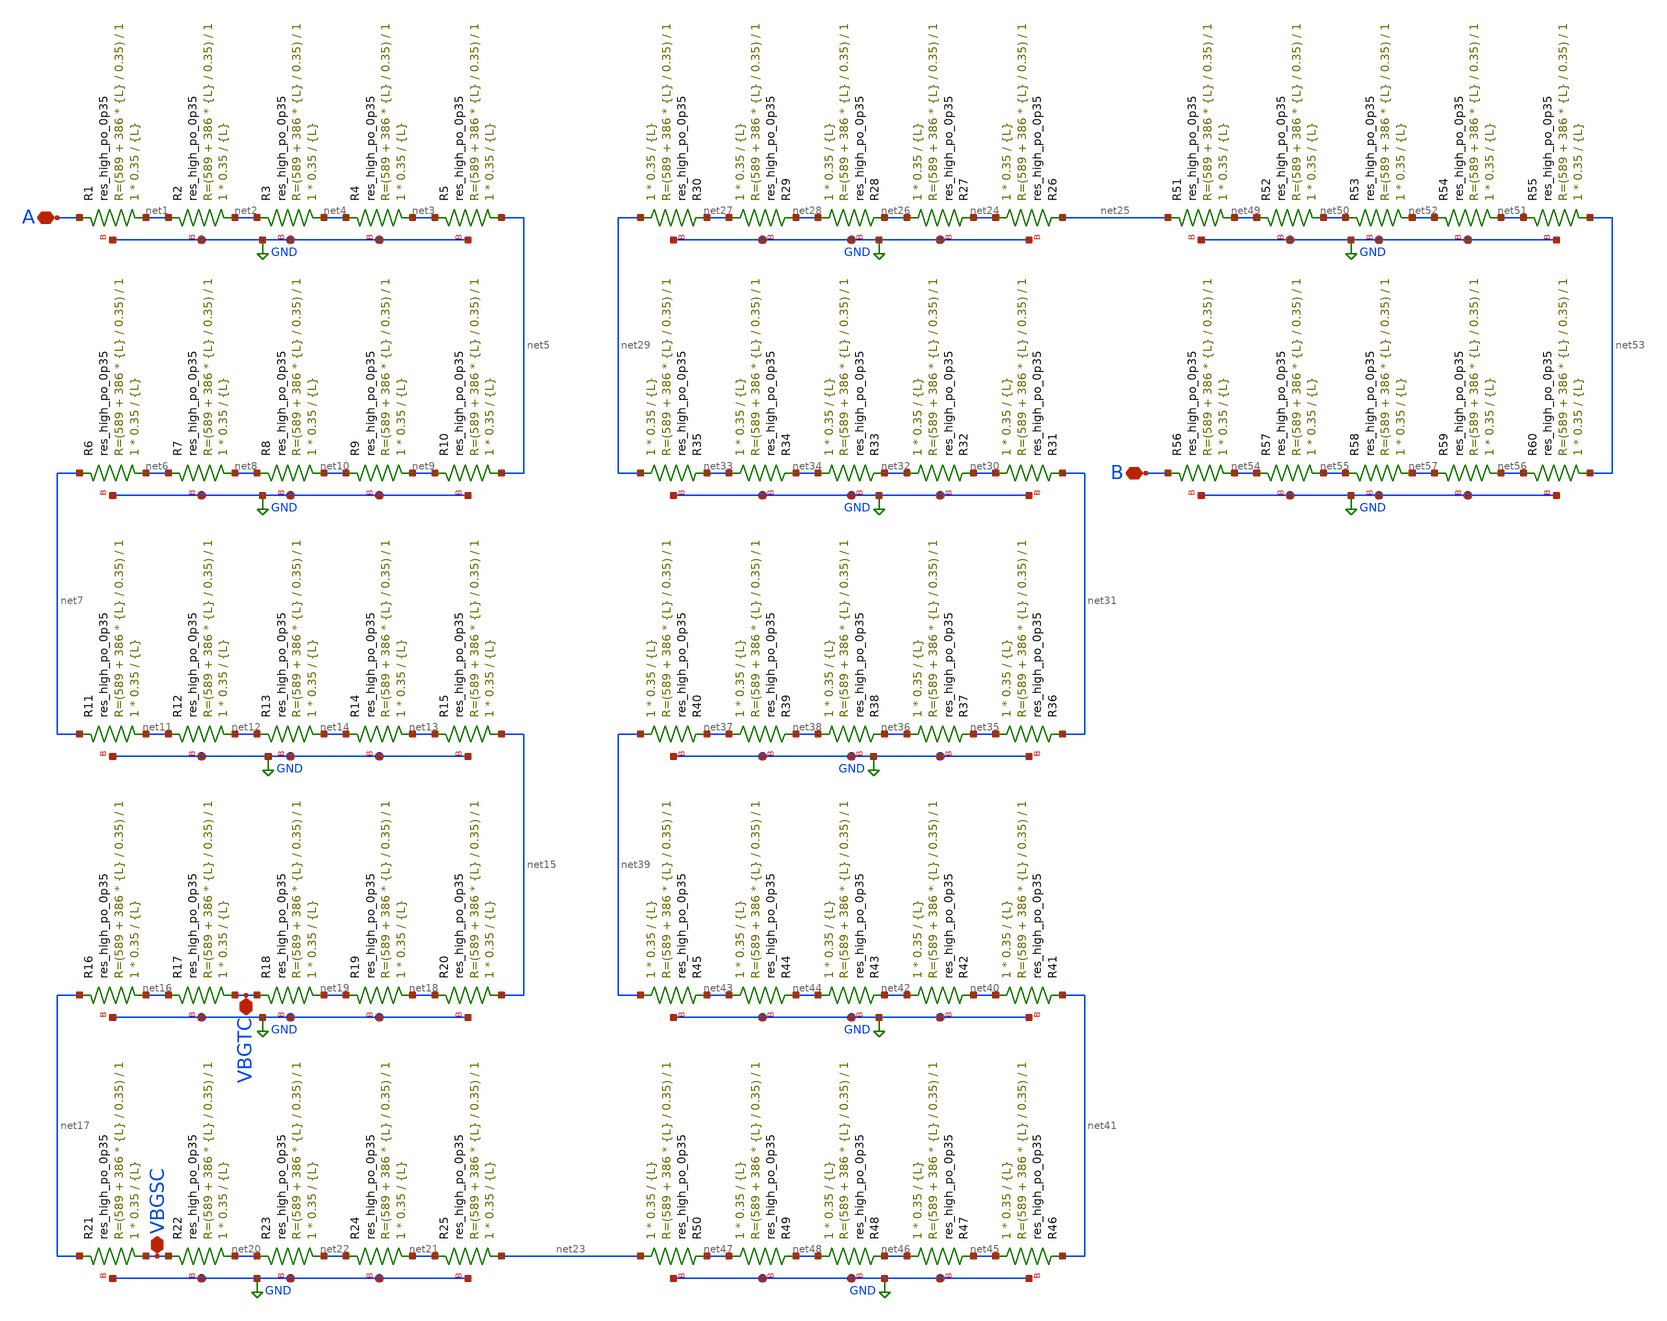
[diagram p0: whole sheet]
** sch_path: xschem/Resistor492k.sch
**.subckt Resistor492k B A VBGTC VBGSC
*.iopin B
*.iopin A
*.iopin VBGTC
*.iopin VBGSC
XR1 net1 A GND sky130_fd_pr__res_high_po_0p35 L={L} mult=1 m=1
XR2 net2 net1 GND sky130_fd_pr__res_high_po_0p35 L={L} mult=1 m=1
XR3 net4 net2 GND sky130_fd_pr__res_high_po_0p35 L={L} mult=1 m=1
XR4 net3 net4 GND sky130_fd_pr__res_high_po_0p35 L={L} mult=1 m=1
XR5 net5 net3 GND sky130_fd_pr__res_high_po_0p35 L={L} mult=1 m=1
XR6 net6 net7 GND sky130_fd_pr__res_high_po_0p35 L={L} mult=1 m=1
XR7 net8 net6 GND sky130_fd_pr__res_high_po_0p35 L={L} mult=1 m=1
XR8 net10 net8 GND sky130_fd_pr__res_high_po_0p35 L={L} mult=1 m=1
XR9 net9 net10 GND sky130_fd_pr__res_high_po_0p35 L={L} mult=1 m=1
XR10 net5 net9 GND sky130_fd_pr__res_high_po_0p35 L={L} mult=1 m=1
XR11 net11 net7 GND sky130_fd_pr__res_high_po_0p35 L={L} mult=1 m=1
XR12 net12 net11 GND sky130_fd_pr__res_high_po_0p35 L={L} mult=1 m=1
XR13 net14 net12 GND sky130_fd_pr__res_high_po_0p35 L={L} mult=1 m=1
XR14 net13 net14 GND sky130_fd_pr__res_high_po_0p35 L={L} mult=1 m=1
XR15 net15 net13 GND sky130_fd_pr__res_high_po_0p35 L={L} mult=1 m=1
XR16 net16 net17 GND sky130_fd_pr__res_high_po_0p35 L={L} mult=1 m=1
XR17 VBGTC net16 GND sky130_fd_pr__res_high_po_0p35 L={L} mult=1 m=1
XR18 net19 VBGTC GND sky130_fd_pr__res_high_po_0p35 L={L} mult=1 m=1
XR19 net18 net19 GND sky130_fd_pr__res_high_po_0p35 L={L} mult=1 m=1
XR20 net15 net18 GND sky130_fd_pr__res_high_po_0p35 L={L} mult=1 m=1
XR21 VBGSC net17 GND sky130_fd_pr__res_high_po_0p35 L={L} mult=1 m=1
XR22 net20 VBGSC GND sky130_fd_pr__res_high_po_0p35 L={L} mult=1 m=1
XR23 net22 net20 GND sky130_fd_pr__res_high_po_0p35 L={L} mult=1 m=1
XR24 net21 net22 GND sky130_fd_pr__res_high_po_0p35 L={L} mult=1 m=1
XR25 net23 net21 GND sky130_fd_pr__res_high_po_0p35 L={L} mult=1 m=1
XR26 net24 net25 GND sky130_fd_pr__res_high_po_0p35 L={L} mult=1 m=1
XR27 net26 net24 GND sky130_fd_pr__res_high_po_0p35 L={L} mult=1 m=1
XR28 net28 net26 GND sky130_fd_pr__res_high_po_0p35 L={L} mult=1 m=1
XR29 net27 net28 GND sky130_fd_pr__res_high_po_0p35 L={L} mult=1 m=1
XR30 net29 net27 GND sky130_fd_pr__res_high_po_0p35 L={L} mult=1 m=1
XR31 net30 net31 GND sky130_fd_pr__res_high_po_0p35 L={L} mult=1 m=1
XR32 net32 net30 GND sky130_fd_pr__res_high_po_0p35 L={L} mult=1 m=1
XR33 net34 net32 GND sky130_fd_pr__res_high_po_0p35 L={L} mult=1 m=1
XR34 net33 net34 GND sky130_fd_pr__res_high_po_0p35 L={L} mult=1 m=1
XR35 net29 net33 GND sky130_fd_pr__res_high_po_0p35 L={L} mult=1 m=1
XR36 net35 net31 GND sky130_fd_pr__res_high_po_0p35 L={L} mult=1 m=1
XR37 net36 net35 GND sky130_fd_pr__res_high_po_0p35 L={L} mult=1 m=1
XR38 net38 net36 GND sky130_fd_pr__res_high_po_0p35 L={L} mult=1 m=1
XR39 net37 net38 GND sky130_fd_pr__res_high_po_0p35 L={L} mult=1 m=1
XR40 net39 net37 GND sky130_fd_pr__res_high_po_0p35 L={L} mult=1 m=1
XR41 net40 net41 GND sky130_fd_pr__res_high_po_0p35 L={L} mult=1 m=1
XR42 net42 net40 GND sky130_fd_pr__res_high_po_0p35 L={L} mult=1 m=1
XR43 net44 net42 GND sky130_fd_pr__res_high_po_0p35 L={L} mult=1 m=1
XR44 net43 net44 GND sky130_fd_pr__res_high_po_0p35 L={L} mult=1 m=1
XR45 net39 net43 GND sky130_fd_pr__res_high_po_0p35 L={L} mult=1 m=1
XR46 net45 net41 GND sky130_fd_pr__res_high_po_0p35 L={L} mult=1 m=1
XR47 net46 net45 GND sky130_fd_pr__res_high_po_0p35 L={L} mult=1 m=1
XR48 net48 net46 GND sky130_fd_pr__res_high_po_0p35 L={L} mult=1 m=1
XR49 net47 net48 GND sky130_fd_pr__res_high_po_0p35 L={L} mult=1 m=1
XR50 net23 net47 GND sky130_fd_pr__res_high_po_0p35 L={L} mult=1 m=1
XR51 net49 net25 GND sky130_fd_pr__res_high_po_0p35 L={L} mult=1 m=1
XR52 net50 net49 GND sky130_fd_pr__res_high_po_0p35 L={L} mult=1 m=1
XR53 net52 net50 GND sky130_fd_pr__res_high_po_0p35 L={L} mult=1 m=1
XR54 net51 net52 GND sky130_fd_pr__res_high_po_0p35 L={L} mult=1 m=1
XR55 net53 net51 GND sky130_fd_pr__res_high_po_0p35 L={L} mult=1 m=1
XR56 net54 B GND sky130_fd_pr__res_high_po_0p35 L={L} mult=1 m=1
XR57 net55 net54 GND sky130_fd_pr__res_high_po_0p35 L={L} mult=1 m=1
XR58 net57 net55 GND sky130_fd_pr__res_high_po_0p35 L={L} mult=1 m=1
XR59 net56 net57 GND sky130_fd_pr__res_high_po_0p35 L={L} mult=1 m=1
XR60 net53 net56 GND sky130_fd_pr__res_high_po_0p35 L={L} mult=1 m=1
**** begin user architecture code


.param L=6.7


**** end user architecture code
**.ends
.GLOBAL GND
.end
